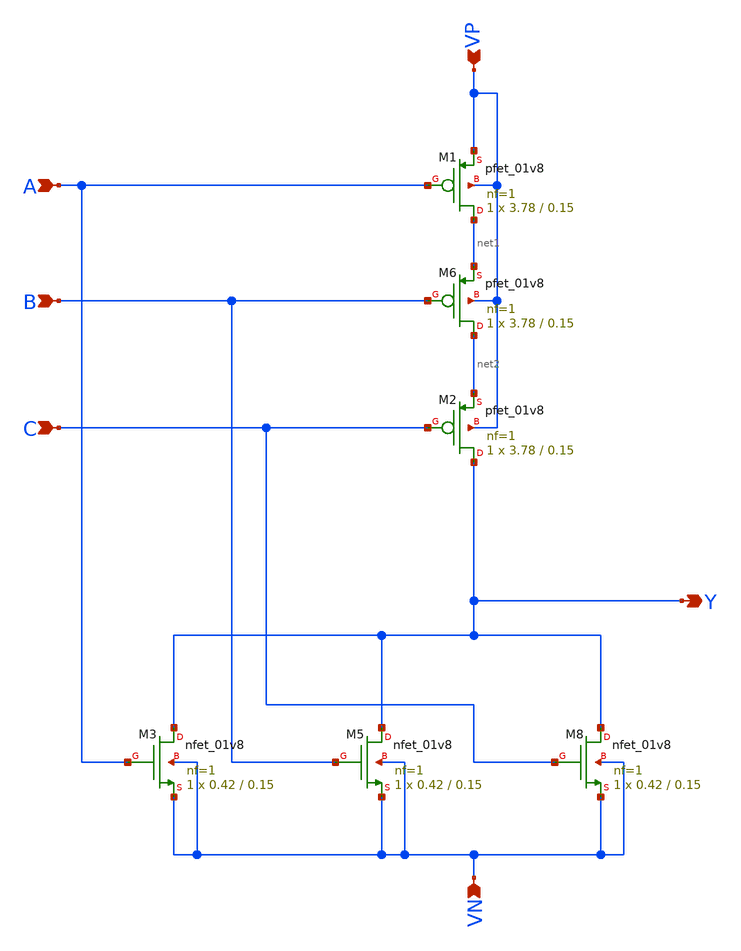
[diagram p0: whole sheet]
** sch_path: component/NOR3/nor3.sch
**.subckt nor3 Y C A B VP VN
*.opin Y
*.ipin C
*.ipin A
*.ipin B
*.ipin VP
*.ipin VN
XM5 Y B VN VN sky130_fd_pr__nfet_01v8 L=0.15 W=0.42 nf=1 ad='int((nf+1)/2) * W/nf * 0.29' as='int((nf+2)/2) * W/nf * 0.29'
+ pd='2*int((nf+1)/2) * (W/nf + 0.29)' ps='2*int((nf+2)/2) * (W/nf + 0.29)' nrd='0.29 / W' nrs='0.29 / W'
+ sa=0 sb=0 sd=0 mult=1 m=1
XM3 Y A VN VN sky130_fd_pr__nfet_01v8 L=0.15 W=0.42 nf=1 ad='int((nf+1)/2) * W/nf * 0.29' as='int((nf+2)/2) * W/nf * 0.29'
+ pd='2*int((nf+1)/2) * (W/nf + 0.29)' ps='2*int((nf+2)/2) * (W/nf + 0.29)' nrd='0.29 / W' nrs='0.29 / W'
+ sa=0 sb=0 sd=0 mult=1 m=1
XM2 Y C net2 VP sky130_fd_pr__pfet_01v8 L=0.15 W=3.78 nf=1 ad='int((nf+1)/2) * W/nf * 0.29' as='int((nf+2)/2) * W/nf * 0.29'
+ pd='2*int((nf+1)/2) * (W/nf + 0.29)' ps='2*int((nf+2)/2) * (W/nf + 0.29)' nrd='0.29 / W' nrs='0.29 / W'
+ sa=0 sb=0 sd=0 mult=1 m=1
XM1 net1 A VP VP sky130_fd_pr__pfet_01v8 L=0.15 W=3.78 nf=1 ad='int((nf+1)/2) * W/nf * 0.29' as='int((nf+2)/2) * W/nf * 0.29'
+ pd='2*int((nf+1)/2) * (W/nf + 0.29)' ps='2*int((nf+2)/2) * (W/nf + 0.29)' nrd='0.29 / W' nrs='0.29 / W'
+ sa=0 sb=0 sd=0 mult=1 m=1
XM6 net2 B net1 VP sky130_fd_pr__pfet_01v8 L=0.15 W=3.78 nf=1 ad='int((nf+1)/2) * W/nf * 0.29' as='int((nf+2)/2) * W/nf * 0.29'
+ pd='2*int((nf+1)/2) * (W/nf + 0.29)' ps='2*int((nf+2)/2) * (W/nf + 0.29)' nrd='0.29 / W' nrs='0.29 / W'
+ sa=0 sb=0 sd=0 mult=1 m=1
XM8 Y C VN VN sky130_fd_pr__nfet_01v8 L=0.15 W=0.42 nf=1 ad='int((nf+1)/2) * W/nf * 0.29' as='int((nf+2)/2) * W/nf * 0.29'
+ pd='2*int((nf+1)/2) * (W/nf + 0.29)' ps='2*int((nf+2)/2) * (W/nf + 0.29)' nrd='0.29 / W' nrs='0.29 / W'
+ sa=0 sb=0 sd=0 mult=1 m=1
**.ends
.end
